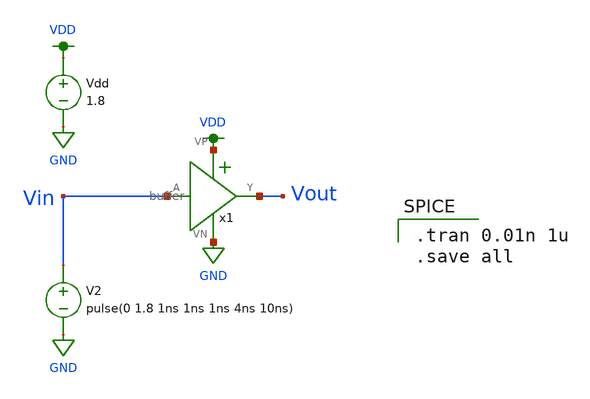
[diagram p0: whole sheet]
** sch_path: mp1/buffer/test_buffer.sch
**.subckt test_buffer
x1 VDD Vin Vout GND buffer
Vdd VDD GND 1.8
V2 Vin GND pulse(0 1.8 1ns 1ns 1ns 4ns 10ns)
**** begin user architecture code

.option wnflag=1
.lib ~/skywater/skywater-pdk/libraries/sky130_fd_pr_ngspice/latest/models/sky130.lib.spice tt


.tran 0.01n 1u
.save all

**** end user architecture code
**.ends

* expanding   symbol:  /home/madvlsi/Documents/vlsi/mp1/buffer/buffer.sym # of pins=4
** sym_path: mp1/buffer/buffer.sym
** sch_path: mp1/buffer/buffer.sch
.subckt buffer VP A Y VN
*.iopin VP
*.iopin VN
*.ipin A
*.opin Y
x1 VP A net1 VN inverter
x2 VP net1 Y VN inverter
.ends


* expanding   symbol:  /home/madvlsi/Documents/vlsi/mp1/inverter/inverter.sym # of pins=4
** sym_path: mp1/inverter/inverter.sym
** sch_path: mp1/inverter/inverter.sch
.subckt inverter VP A Y VN
*.iopin VP
*.iopin VN
*.ipin A
*.opin Y
XM1 Y A VN VN sky130_fd_pr__nfet_01v8 L=0.15 W=1 nf=1 ad='int((nf+1)/2) * W/nf * 0.29' as='int((nf+2)/2) * W/nf * 0.29'
+ pd='2*int((nf+1)/2) * (W/nf + 0.29)' ps='2*int((nf+2)/2) * (W/nf + 0.29)' nrd='0.29 / W' nrs='0.29 / W'
+ sa=0 sb=0 sd=0 mult=1 m=1
XM2 Y A VP VP sky130_fd_pr__pfet_01v8 L=0.15 W=1 nf=1 ad='int((nf+1)/2) * W/nf * 0.29' as='int((nf+2)/2) * W/nf * 0.29'
+ pd='2*int((nf+1)/2) * (W/nf + 0.29)' ps='2*int((nf+2)/2) * (W/nf + 0.29)' nrd='0.29 / W' nrs='0.29 / W'
+ sa=0 sb=0 sd=0 mult=1 m=1
.ends

.GLOBAL VDD
.GLOBAL GND
.end
